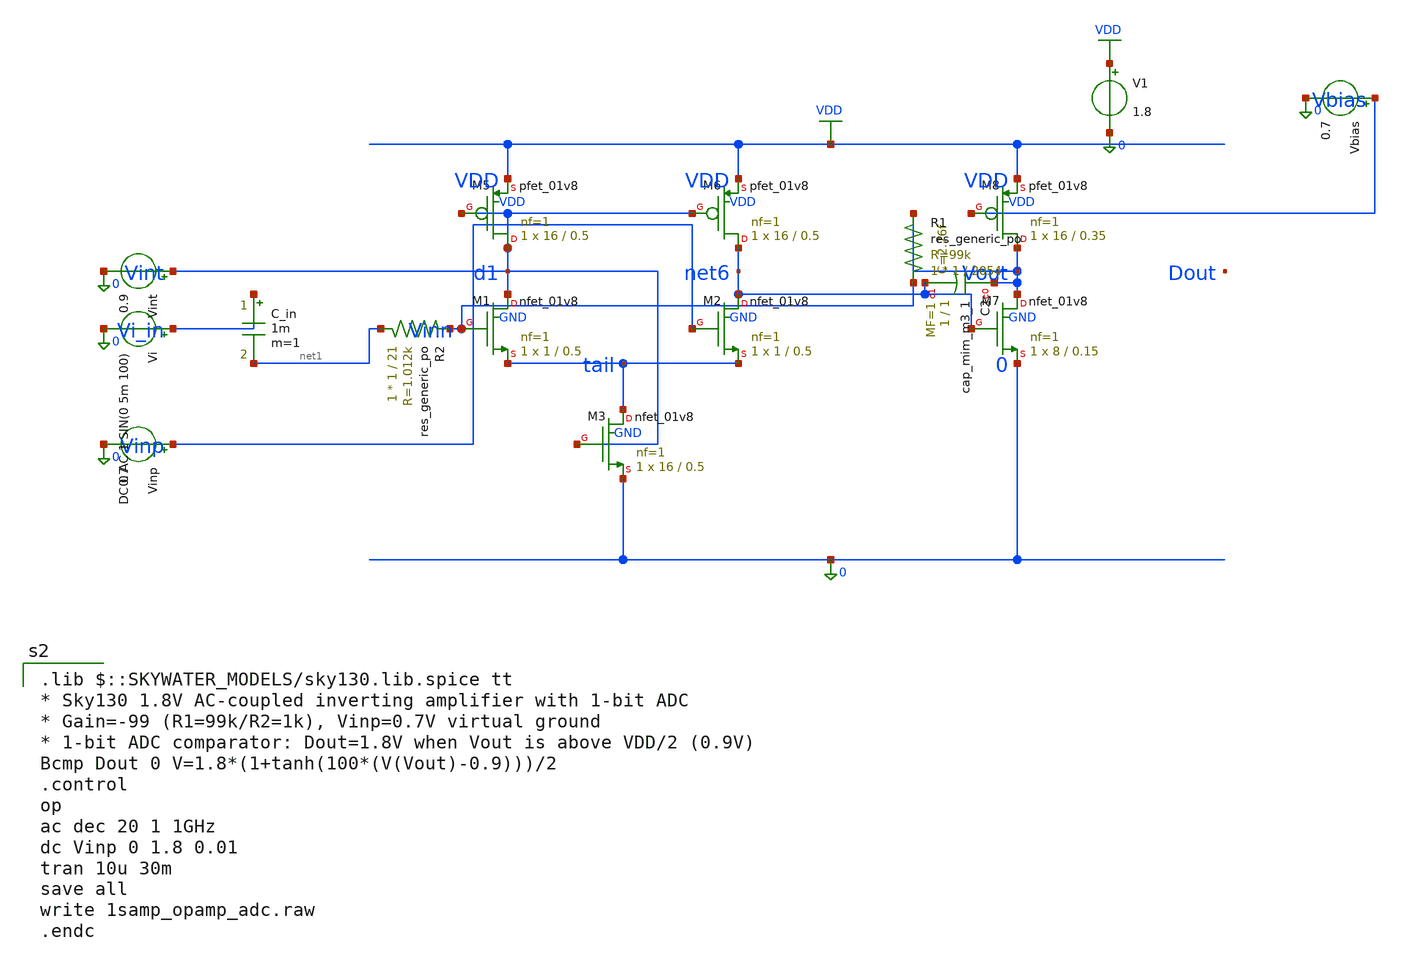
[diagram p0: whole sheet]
** sch_path: first_tapeout_eeg/source/trials/20260730/1samp_opamp_adc.sch
**.subckt 1samp_opamp_adc
V1 VDD 0 1.8
Vinp Vinp 0 0.7
Vint Vint 0 0.9
Vbias Vbias 0 0.7
XM1 d1 Vinn tail GND sky130_fd_pr__nfet_01v8 L=0.5 W=1 nf=1 ad='int((nf+1)/2) * W/nf * 0.29' as='int((nf+2)/2) * W/nf * 0.29'
+ pd='2*int((nf+1)/2) * (W/nf + 0.29)' ps='2*int((nf+2)/2) * (W/nf + 0.29)' nrd='0.29 / W' nrs='0.29 / W'
+ sa=0 sb=0 sd=0 mult=1 m=1
XM2 net6 Vinp tail GND sky130_fd_pr__nfet_01v8 L=0.5 W=1 nf=1 ad='int((nf+1)/2) * W/nf * 0.29' as='int((nf+2)/2) * W/nf * 0.29'
+ pd='2*int((nf+1)/2) * (W/nf + 0.29)' ps='2*int((nf+2)/2) * (W/nf + 0.29)' nrd='0.29 / W' nrs='0.29 / W'
+ sa=0 sb=0 sd=0 mult=1 m=1
XM3 tail Vint 0 GND sky130_fd_pr__nfet_01v8 L=0.5 W=16 nf=1 ad='int((nf+1)/2) * W/nf * 0.29' as='int((nf+2)/2) * W/nf * 0.29'
+ pd='2*int((nf+1)/2) * (W/nf + 0.29)' ps='2*int((nf+2)/2) * (W/nf + 0.29)' nrd='0.29 / W' nrs='0.29 / W'
+ sa=0 sb=0 sd=0 mult=1 m=1
XM5 d1 d1 VDD VDD sky130_fd_pr__pfet_01v8 L=0.5 W=16 nf=1 ad='int((nf+1)/2) * W/nf * 0.29' as='int((nf+2)/2) * W/nf * 0.29'
+ pd='2*int((nf+1)/2) * (W/nf + 0.29)' ps='2*int((nf+2)/2) * (W/nf + 0.29)' nrd='0.29 / W' nrs='0.29 / W'
+ sa=0 sb=0 sd=0 mult=1 m=1
XM6 net6 d1 VDD VDD sky130_fd_pr__pfet_01v8 L=0.5 W=16 nf=1 ad='int((nf+1)/2) * W/nf * 0.29' as='int((nf+2)/2) * W/nf * 0.29'
+ pd='2*int((nf+1)/2) * (W/nf + 0.29)' ps='2*int((nf+2)/2) * (W/nf + 0.29)' nrd='0.29 / W' nrs='0.29 / W'
+ sa=0 sb=0 sd=0 mult=1 m=1
XM7 Vout net6 0 GND sky130_fd_pr__nfet_01v8 L=0.15 W=8 nf=1 ad='int((nf+1)/2) * W/nf * 0.29' as='int((nf+2)/2) * W/nf * 0.29'
+ pd='2*int((nf+1)/2) * (W/nf + 0.29)' ps='2*int((nf+2)/2) * (W/nf + 0.29)' nrd='0.29 / W' nrs='0.29 / W'
+ sa=0 sb=0 sd=0 mult=1 m=1
XM8 Vout Vbias VDD VDD sky130_fd_pr__pfet_01v8 L=0.35 W=16 nf=1 ad='int((nf+1)/2) * W/nf * 0.29' as='int((nf+2)/2) * W/nf * 0.29'
+ pd='2*int((nf+1)/2) * (W/nf + 0.29)' ps='2*int((nf+2)/2) * (W/nf + 0.29)' nrd='0.29 / W' nrs='0.29 / W'
+ sa=0 sb=0 sd=0 mult=1 m=1
XC2 Vout net6 sky130_fd_pr__cap_mim_m3_1 W=1 L=1 MF=1 m=1
XR1 Vinn Vout sky130_fd_pr__res_generic_po W=1 L=2054 m=1
XR2 net1 Vinn sky130_fd_pr__res_generic_po W=1 L=21 m=1
Vi Vi_in 0 DC 0 AC 1 SIN(0 5m 100)
C_in Vi_in net1 1m m=1
**** begin user architecture code
 .lib $::SKYWATER_MODELS/sky130.lib.spice tt
* Sky130 1.8V AC-coupled inverting amplifier with 1-bit ADC
* Gain=-99 (R1=99k/R2=1k), Vinp=0.7V virtual ground
* 1-bit ADC comparator: Dout=1.8V when Vout is above VDD/2 (0.9V)
Bcmp Dout 0 V=1.8*(1+tanh(100*(V(Vout)-0.9)))/2
.control
op
ac dec 20 1 1GHz
dc Vinp 0 1.8 0.01
tran 10u 30m
save all
write 1samp_opamp_adc.raw
.endc
**** end user architecture code
**.ends
.GLOBAL VDD
.end
